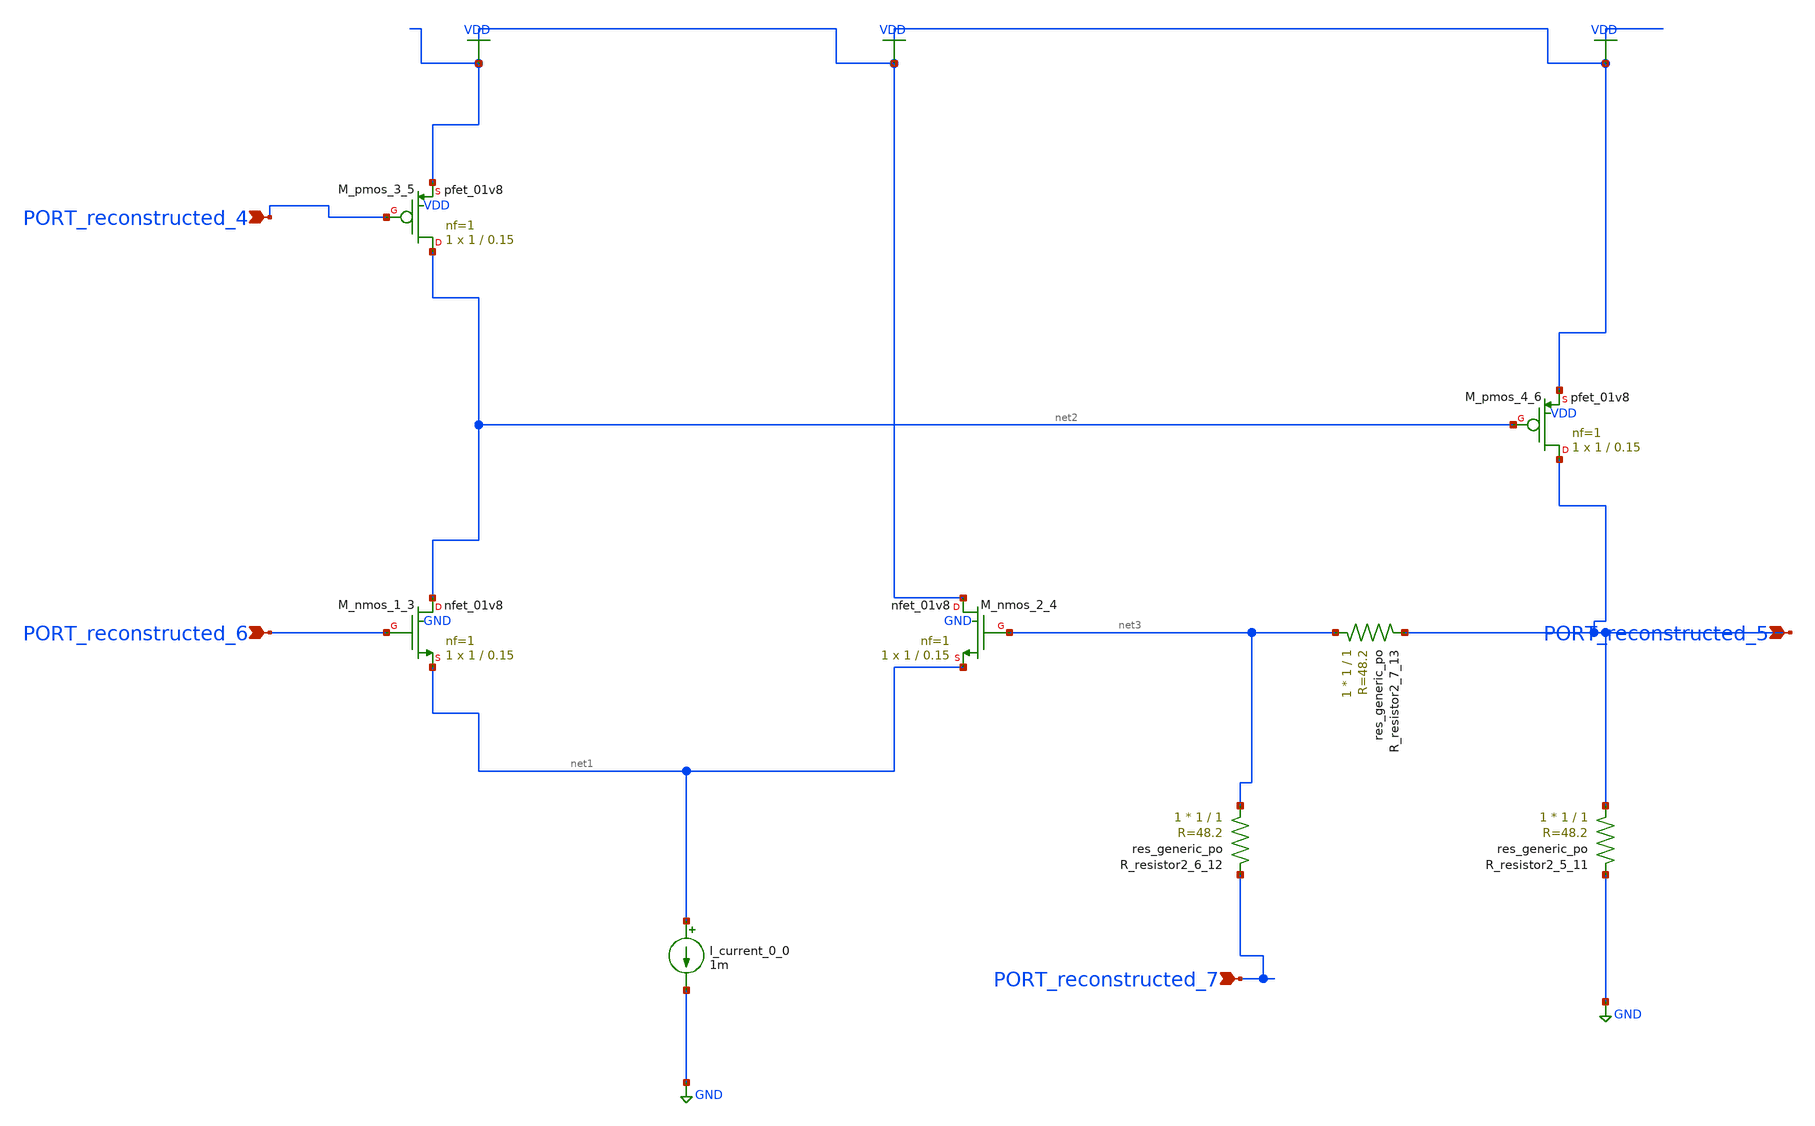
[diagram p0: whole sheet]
** sch_path: schematics/AMSNet/616.sch
**.subckt 616 PORT_reconstructed_6 PORT_reconstructed_5 PORT_reconstructed_4 PORT_reconstructed_7
*.ipin PORT_reconstructed_6
*.ipin PORT_reconstructed_5
*.ipin PORT_reconstructed_4
*.ipin PORT_reconstructed_7
I_current_0_0 net1 GND 1m
XM_nmos_1_3 net2 PORT_reconstructed_6 net1 GND sky130_fd_pr__nfet_01v8 L=0.15 W=1 nf=1 ad='int((1 + 1)/2) * 1 / 1 * 0.29'
+ as='int((1 + 2)/2) * 1 / 1 * 0.29' pd='2*int((1 + 1)/2) * (1 / 1 + 0.29)' ps='2*int((1 + 2)/2) * (1 / 1 + 0.29)'
+ nrd='0.29 / 1 ' nrs='0.29 / 1 ' sa=0 sb=0 sd=0 mult=1 m=1
XM_nmos_2_4 VDD net3 net1 GND sky130_fd_pr__nfet_01v8 L=0.15 W=1 nf=1 ad='int((1 + 1)/2) * 1 / 1 * 0.29'
+ as='int((1 + 2)/2) * 1 / 1 * 0.29' pd='2*int((1 + 1)/2) * (1 / 1 + 0.29)' ps='2*int((1 + 2)/2) * (1 / 1 + 0.29)'
+ nrd='0.29 / 1 ' nrs='0.29 / 1 ' sa=0 sb=0 sd=0 mult=1 m=1
XM_pmos_3_5 net2 PORT_reconstructed_4 VDD VDD sky130_fd_pr__pfet_01v8 L=0.15 W=1 nf=1 ad='int((1 + 1)/2) * 1 / 1 * 0.29'
+ as='int((1 + 2)/2) * 1 / 1 * 0.29' pd='2*int((1 + 1)/2) * (1 / 1 + 0.29)' ps='2*int((1 + 2)/2) * (1 / 1 + 0.29)'
+ nrd='0.29 / 1 ' nrs='0.29 / 1 ' sa=0 sb=0 sd=0 mult=1 m=1
XM_pmos_4_6 PORT_reconstructed_5 net2 VDD VDD sky130_fd_pr__pfet_01v8 L=0.15 W=1 nf=1 ad='int((1 + 1)/2) * 1 / 1 * 0.29'
+ as='int((1 + 2)/2) * 1 / 1 * 0.29' pd='2*int((1 + 1)/2) * (1 / 1 + 0.29)' ps='2*int((1 + 2)/2) * (1 / 1 + 0.29)'
+ nrd='0.29 / 1 ' nrs='0.29 / 1 ' sa=0 sb=0 sd=0 mult=1 m=1
XR_resistor2_5_11 PORT_reconstructed_5 GND sky130_fd_pr__res_generic_po W=1 L=1 m=1
XR_resistor2_6_12 net3 PORT_reconstructed_7 sky130_fd_pr__res_generic_po W=1 L=1 m=1
XR_resistor2_7_13 net3 PORT_reconstructed_5 sky130_fd_pr__res_generic_po W=1 L=1 m=1
**.ends
.GLOBAL GND
.GLOBAL VDD
.end
